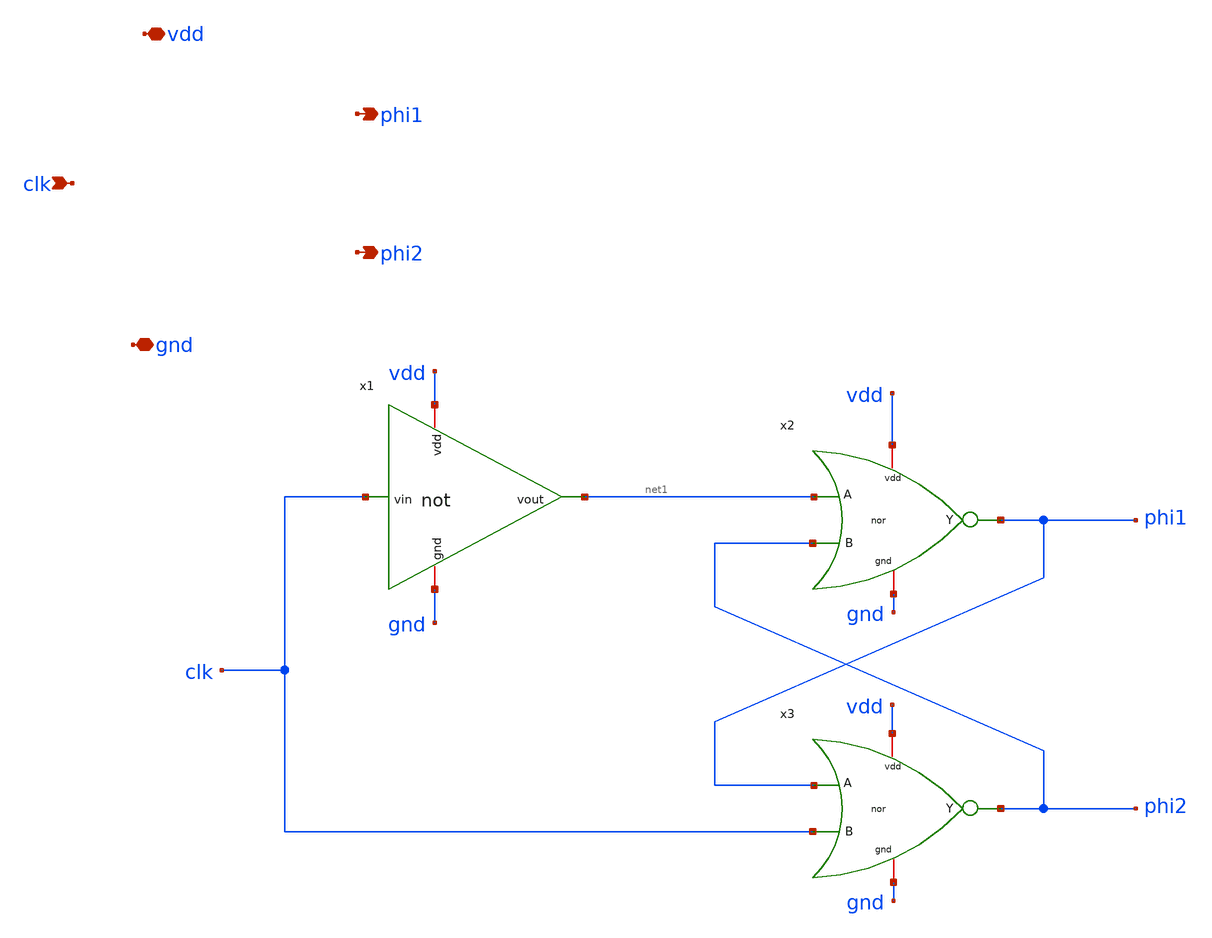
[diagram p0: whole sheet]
** sch_path: SequentialCircuits/Non Overlapping Clock Generator/non_overlapping_clk_gen.sch
**.subckt non_overlapping_clk_gen clk vdd gnd phi1 phi2
*.ipin clk
*.iopin vdd
*.iopin gnd
*.opin phi1
*.opin phi2
x1 vdd gnd clk net1 not
x2 vdd gnd net1 phi2 phi1 nor
x3 vdd gnd phi1 clk phi2 nor
**.ends

* expanding   symbol:  LogicGates/not.sym # of pins=4
** sym_path: LogicGates/not.sym
** sch_path: LogicGates/not.sch
.subckt not vdd gnd vin vout
*.ipin vin
*.iopin vdd
*.iopin gnd
*.opin vout
XM2 vout vin vdd vdd sky130_fd_pr__pfet_01v8 L=0.15 W=2 nf=1 ad='int((nf+1)/2) * W/nf * 0.29' as='int((nf+2)/2) * W/nf * 0.29'
+ pd='2*int((nf+1)/2) * (W/nf + 0.29)' ps='2*int((nf+2)/2) * (W/nf + 0.29)' nrd='0.29 / W' nrs='0.29 / W'
+ sa=0 sb=0 sd=0 mult=1 m=1
XM1 vout vin gnd gnd sky130_fd_pr__nfet_01v8 L=0.15 W=1 nf=1 ad='int((nf+1)/2) * W/nf * 0.29' as='int((nf+2)/2) * W/nf * 0.29'
+ pd='2*int((nf+1)/2) * (W/nf + 0.29)' ps='2*int((nf+2)/2) * (W/nf + 0.29)' nrd='0.29 / W' nrs='0.29 / W'
+ sa=0 sb=0 sd=0 mult=1 m=1
.ends


* expanding   symbol:  LogicGates/nor.sym # of pins=5
** sym_path: LogicGates/nor.sym
** sch_path: LogicGates/nor.sch
.subckt nor vdd gnd A B Y
*.ipin A
*.ipin B
*.iopin vdd
*.iopin gnd
*.opin Y
XM1 Y A gnd gnd sky130_fd_pr__nfet_01v8 L=0.15 W=1 nf=1 ad='int((nf+1)/2) * W/nf * 0.29' as='int((nf+2)/2) * W/nf * 0.29'
+ pd='2*int((nf+1)/2) * (W/nf + 0.29)' ps='2*int((nf+2)/2) * (W/nf + 0.29)' nrd='0.29 / W' nrs='0.29 / W'
+ sa=0 sb=0 sd=0 mult=1 m=1
XM2 Y B gnd gnd sky130_fd_pr__nfet_01v8 L=0.15 W=1 nf=1 ad='int((nf+1)/2) * W/nf * 0.29' as='int((nf+2)/2) * W/nf * 0.29'
+ pd='2*int((nf+1)/2) * (W/nf + 0.29)' ps='2*int((nf+2)/2) * (W/nf + 0.29)' nrd='0.29 / W' nrs='0.29 / W'
+ sa=0 sb=0 sd=0 mult=1 m=1
XM3 net1 A vdd vdd sky130_fd_pr__pfet_01v8 L=0.15 W=2 nf=1 ad='int((nf+1)/2) * W/nf * 0.29' as='int((nf+2)/2) * W/nf * 0.29'
+ pd='2*int((nf+1)/2) * (W/nf + 0.29)' ps='2*int((nf+2)/2) * (W/nf + 0.29)' nrd='0.29 / W' nrs='0.29 / W'
+ sa=0 sb=0 sd=0 mult=1 m=1
XM4 Y B net1 vdd sky130_fd_pr__pfet_01v8 L=0.15 W=2 nf=1 ad='int((nf+1)/2) * W/nf * 0.29' as='int((nf+2)/2) * W/nf * 0.29'
+ pd='2*int((nf+1)/2) * (W/nf + 0.29)' ps='2*int((nf+2)/2) * (W/nf + 0.29)' nrd='0.29 / W' nrs='0.29 / W'
+ sa=0 sb=0 sd=0 mult=1 m=1
.ends

.end
